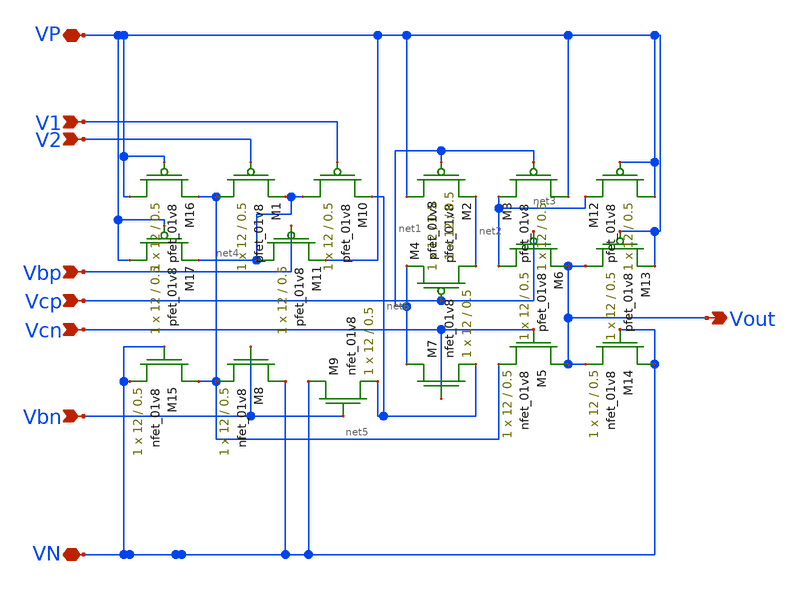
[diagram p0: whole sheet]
** sch_path: MiniProject3-Cascode/XSCHEM/fcascodediffamp.sch
**.subckt fcascodediffamp VP VN V1 V2 Vbp Vcp Vcn Vbn Vout
*.iopin VP
*.iopin VN
*.ipin V1
*.ipin V2
*.ipin Vbp
*.ipin Vcp
*.ipin Vcn
*.ipin Vbn
*.opin Vout
XM5 Vout Vcn net5 GND sky130_fd_pr__nfet_01v8 L=0.5 W=12 nf=1 ad='int((nf+1)/2) * W/nf * 0.29' as='int((nf+2)/2) * W/nf * 0.29'
+ pd='2*int((nf+1)/2) * (W/nf + 0.29)' ps='2*int((nf+2)/2) * (W/nf + 0.29)' nrd='0.29 / W' nrs='0.29 / W'
+ sa=0 sb=0 sd=0 mult=1 m=1
XM2 VP net1 net2 VDD sky130_fd_pr__pfet_01v8 L=0.5 W=12 nf=1 ad='int((nf+1)/2) * W/nf * 0.29' as='int((nf+2)/2) * W/nf * 0.29'
+ pd='2*int((nf+1)/2) * (W/nf + 0.29)' ps='2*int((nf+2)/2) * (W/nf + 0.29)' nrd='0.29 / W' nrs='0.29 / W'
+ sa=0 sb=0 sd=0 mult=1 m=1
XM3 VP net1 net3 VDD sky130_fd_pr__pfet_01v8 L=0.5 W=12 nf=1 ad='int((nf+1)/2) * W/nf * 0.29' as='int((nf+2)/2) * W/nf * 0.29'
+ pd='2*int((nf+1)/2) * (W/nf + 0.29)' ps='2*int((nf+2)/2) * (W/nf + 0.29)' nrd='0.29 / W' nrs='0.29 / W'
+ sa=0 sb=0 sd=0 mult=1 m=1
XM4 net2 Vcp net1 VDD sky130_fd_pr__pfet_01v8 L=0.5 W=12 nf=1 ad='int((nf+1)/2) * W/nf * 0.29' as='int((nf+2)/2) * W/nf * 0.29'
+ pd='2*int((nf+1)/2) * (W/nf + 0.29)' ps='2*int((nf+2)/2) * (W/nf + 0.29)' nrd='0.29 / W' nrs='0.29 / W'
+ sa=0 sb=0 sd=0 mult=1 m=1
XM6 net3 Vcp Vout VDD sky130_fd_pr__pfet_01v8 L=0.5 W=12 nf=1 ad='int((nf+1)/2) * W/nf * 0.29' as='int((nf+2)/2) * W/nf * 0.29'
+ pd='2*int((nf+1)/2) * (W/nf + 0.29)' ps='2*int((nf+2)/2) * (W/nf + 0.29)' nrd='0.29 / W' nrs='0.29 / W'
+ sa=0 sb=0 sd=0 mult=1 m=1
XM7 net1 Vcn net6 GND sky130_fd_pr__nfet_01v8 L=0.5 W=12 nf=1 ad='int((nf+1)/2) * W/nf * 0.29' as='int((nf+2)/2) * W/nf * 0.29'
+ pd='2*int((nf+1)/2) * (W/nf + 0.29)' ps='2*int((nf+2)/2) * (W/nf + 0.29)' nrd='0.29 / W' nrs='0.29 / W'
+ sa=0 sb=0 sd=0 mult=1 m=1
XM8 VN Vbn net5 GND sky130_fd_pr__nfet_01v8 L=0.5 W=12 nf=1 ad='int((nf+1)/2) * W/nf * 0.29' as='int((nf+2)/2) * W/nf * 0.29'
+ pd='2*int((nf+1)/2) * (W/nf + 0.29)' ps='2*int((nf+2)/2) * (W/nf + 0.29)' nrd='0.29 / W' nrs='0.29 / W'
+ sa=0 sb=0 sd=0 mult=1 m=1
XM9 VN Vbn net6 GND sky130_fd_pr__nfet_01v8 L=0.5 W=12 nf=1 ad='int((nf+1)/2) * W/nf * 0.29' as='int((nf+2)/2) * W/nf * 0.29'
+ pd='2*int((nf+1)/2) * (W/nf + 0.29)' ps='2*int((nf+2)/2) * (W/nf + 0.29)' nrd='0.29 / W' nrs='0.29 / W'
+ sa=0 sb=0 sd=0 mult=1 m=1
XM10 net4 V1 net6 VDD sky130_fd_pr__pfet_01v8 L=0.5 W=12 nf=1 ad='int((nf+1)/2) * W/nf * 0.29' as='int((nf+2)/2) * W/nf * 0.29'
+ pd='2*int((nf+1)/2) * (W/nf + 0.29)' ps='2*int((nf+2)/2) * (W/nf + 0.29)' nrd='0.29 / W' nrs='0.29 / W'
+ sa=0 sb=0 sd=0 mult=1 m=1
XM1 net5 V2 net4 VDD sky130_fd_pr__pfet_01v8 L=0.5 W=12 nf=1 ad='int((nf+1)/2) * W/nf * 0.29' as='int((nf+2)/2) * W/nf * 0.29'
+ pd='2*int((nf+1)/2) * (W/nf + 0.29)' ps='2*int((nf+2)/2) * (W/nf + 0.29)' nrd='0.29 / W' nrs='0.29 / W'
+ sa=0 sb=0 sd=0 mult=1 m=1
XM11 net4 Vbp VP VDD sky130_fd_pr__pfet_01v8 L=0.5 W=12 nf=1 ad='int((nf+1)/2) * W/nf * 0.29' as='int((nf+2)/2) * W/nf * 0.29'
+ pd='2*int((nf+1)/2) * (W/nf + 0.29)' ps='2*int((nf+2)/2) * (W/nf + 0.29)' nrd='0.29 / W' nrs='0.29 / W'
+ sa=0 sb=0 sd=0 mult=1 m=1
XM12 VP VP net3 VDD sky130_fd_pr__pfet_01v8 L=0.5 W=12 nf=1 ad='int((nf+1)/2) * W/nf * 0.29' as='int((nf+2)/2) * W/nf * 0.29'
+ pd='2*int((nf+1)/2) * (W/nf + 0.29)' ps='2*int((nf+2)/2) * (W/nf + 0.29)' nrd='0.29 / W' nrs='0.29 / W'
+ sa=0 sb=0 sd=0 mult=1 m=1
XM13 Vout VP VP VDD sky130_fd_pr__pfet_01v8 L=0.5 W=12 nf=1 ad='int((nf+1)/2) * W/nf * 0.29' as='int((nf+2)/2) * W/nf * 0.29'
+ pd='2*int((nf+1)/2) * (W/nf + 0.29)' ps='2*int((nf+2)/2) * (W/nf + 0.29)' nrd='0.29 / W' nrs='0.29 / W'
+ sa=0 sb=0 sd=0 mult=1 m=1
XM14 VN VN Vout GND sky130_fd_pr__nfet_01v8 L=0.5 W=12 nf=1 ad='int((nf+1)/2) * W/nf * 0.29' as='int((nf+2)/2) * W/nf * 0.29'
+ pd='2*int((nf+1)/2) * (W/nf + 0.29)' ps='2*int((nf+2)/2) * (W/nf + 0.29)' nrd='0.29 / W' nrs='0.29 / W'
+ sa=0 sb=0 sd=0 mult=1 m=1
XM15 net5 VN VN GND sky130_fd_pr__nfet_01v8 L=0.5 W=12 nf=1 ad='int((nf+1)/2) * W/nf * 0.29' as='int((nf+2)/2) * W/nf * 0.29'
+ pd='2*int((nf+1)/2) * (W/nf + 0.29)' ps='2*int((nf+2)/2) * (W/nf + 0.29)' nrd='0.29 / W' nrs='0.29 / W'
+ sa=0 sb=0 sd=0 mult=1 m=1
XM16 VP VP net5 VDD sky130_fd_pr__pfet_01v8 L=0.5 W=12 nf=1 ad='int((nf+1)/2) * W/nf * 0.29' as='int((nf+2)/2) * W/nf * 0.29'
+ pd='2*int((nf+1)/2) * (W/nf + 0.29)' ps='2*int((nf+2)/2) * (W/nf + 0.29)' nrd='0.29 / W' nrs='0.29 / W'
+ sa=0 sb=0 sd=0 mult=1 m=1
XM17 VP VP net4 VDD sky130_fd_pr__pfet_01v8 L=0.5 W=12 nf=1 ad='int((nf+1)/2) * W/nf * 0.29' as='int((nf+2)/2) * W/nf * 0.29'
+ pd='2*int((nf+1)/2) * (W/nf + 0.29)' ps='2*int((nf+2)/2) * (W/nf + 0.29)' nrd='0.29 / W' nrs='0.29 / W'
+ sa=0 sb=0 sd=0 mult=1 m=1
**.ends
.end
